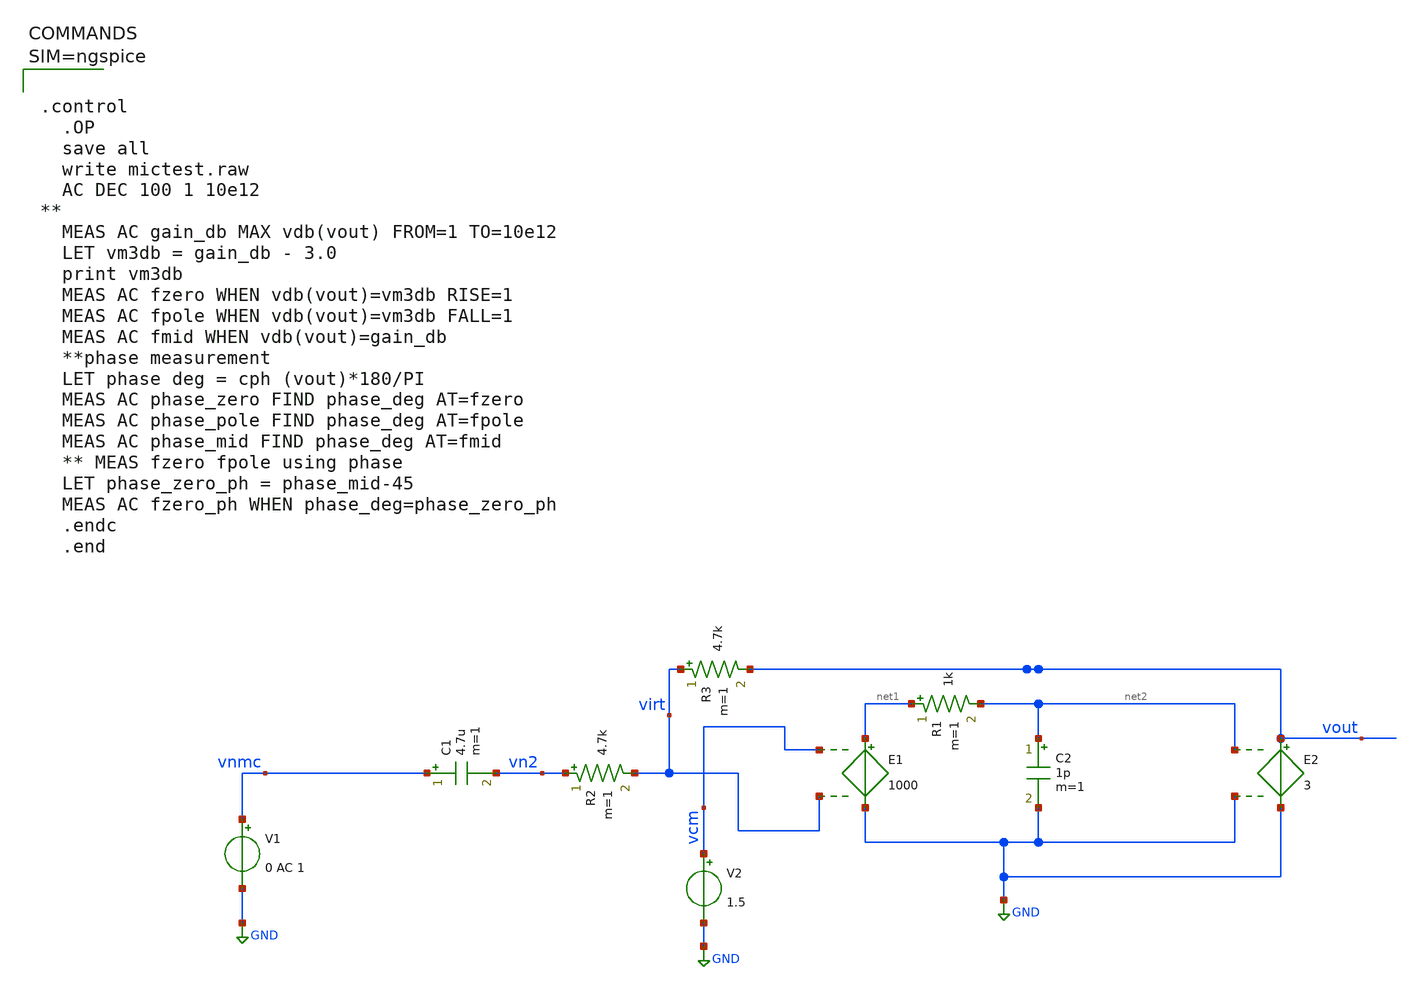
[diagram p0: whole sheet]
** sch_path: xschem/bandpass.sch
**.subckt bandpass
V1 vnmc GND 0 AC 1
C1 vnmc vn2 4.7u m=1
R2 vn2 virt 4.7k m=1
R3 virt vout 4.7k m=1
V2 vcm GND 1.5
E1 net1 GND vcm virt 1000
E2 vout GND net2 GND 3
C2 net2 GND 1p m=1
R1 net1 net2 1k m=1
**** begin user architecture code



.control
  .OP
  save all
  write mictest.raw
  AC DEC 100 1 10e12
**
  MEAS AC gain_db MAX vdb(vout) FROM=1 TO=10e12
  LET vm3db = gain_db - 3.0
  print vm3db
  MEAS AC fzero WHEN vdb(vout)=vm3db RISE=1
  MEAS AC fpole WHEN vdb(vout)=vm3db FALL=1
  MEAS AC fmid WHEN vdb(vout)=gain_db
  **phase measurement
  LET phase deg = cph (vout)*180/PI
  MEAS AC phase_zero FIND phase_deg AT=fzero
  MEAS AC phase_pole FIND phase_deg AT=fpole
  MEAS AC phase_mid FIND phase_deg AT=fmid
  ** MEAS fzero fpole using phase
  LET phase_zero_ph = phase_mid-45
  MEAS AC fzero_ph WHEN phase_deg=phase_zero_ph
  .endc
  .end




**** end user architecture code
**.ends
.GLOBAL GND
.end
